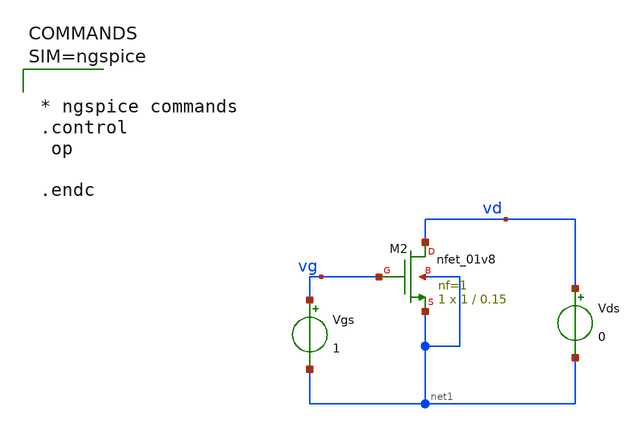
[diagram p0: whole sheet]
** sch_path: xschem/nfet_M2.sch
**.subckt nfet_M2
Vgs vg net1 1
Vds vd net1 0
XM2 vd vg net1 net1 sky130_fd_pr__nfet_01v8 L=0.15 W=1 nf=1 ad='int((1 + 1)/2) * 1 / 1 * 0.29' as='int((1 + 2)/2) * 1 / 1 * 0.29'
+ pd='2*int((1 + 1)/2) * (1 / 1 + 0.29)' ps='2*int((1 + 2)/2) * (1 / 1 + 0.29)' nrd='0.29 / 1 ' nrs='0.29 / 1 '
+ sa=0 sb=0 sd=0 mult=1 m=1
**** begin user architecture code

** opencircuitdesign pdks install
.lib $::SKYWATER_MODELS/sky130.lib.spice tt




* ngspice commands
.control
 op

.endc



**** end user architecture code
**.ends
.end
